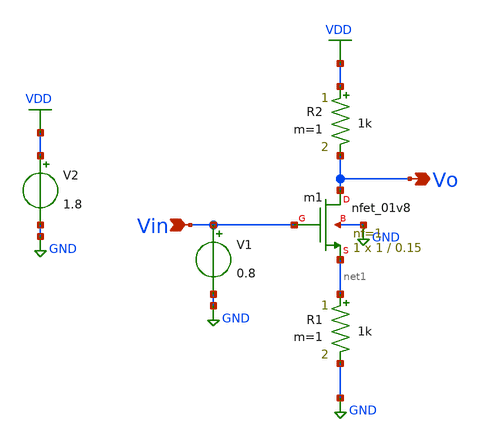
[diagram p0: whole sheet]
** sch_path: SINGLE_STAGE_AMP/CS_DEGENERATION/degeneration.sch
**.subckt degeneration Vin Vo
*.ipin Vin
*.opin Vo
R1 net1 GND 1k m=1
R2 VDD Vo 1k m=1
V1 Vin GND 0.8
V2 VDD GND 1.8
Xm1 Vo Vin net1 GND sky130_fd_pr__nfet_01v8 L=0.15 W=1 nf=1 ad='int((nf+1)/2) * W/nf * 0.29' as='int((nf+2)/2) * W/nf * 0.29'
+ pd='2*int((nf+1)/2) * (W/nf + 0.29)' ps='2*int((nf+2)/2) * (W/nf + 0.29)' nrd='0.29 / W' nrs='0.29 / W'
+ sa=0 sb=0 sd=0 mult=1 m=1
**** begin user architecture code


.lib /home/varun/.ciel/ciel/sky130/versions/1689ac3f2dc763876eaf967227c7dfe831b031ae/sky130A/libs.tech/ngspice/sky130.lib.spice tt
.dc V1 0 1.8 10u
.save all



**** end user architecture code
**.ends
.GLOBAL VDD
.GLOBAL GND
.end
